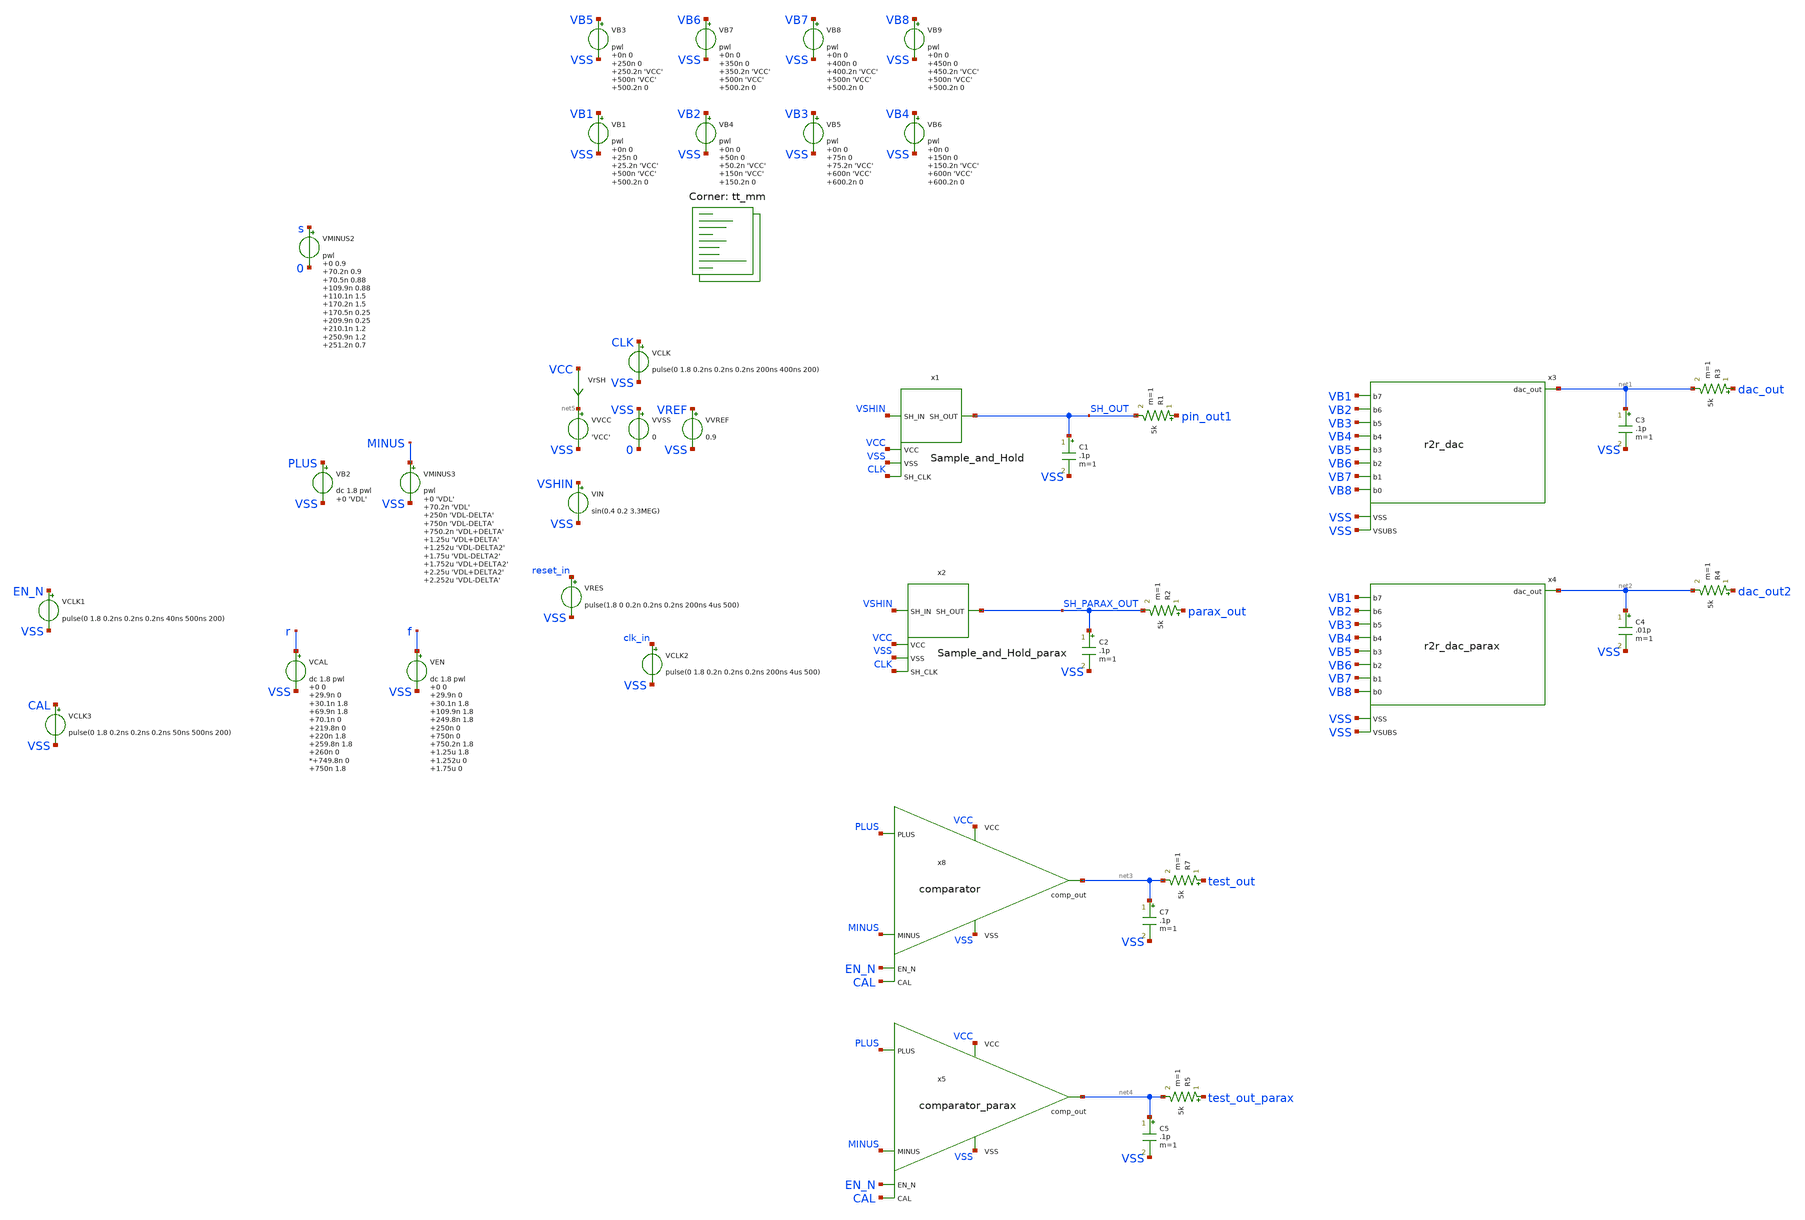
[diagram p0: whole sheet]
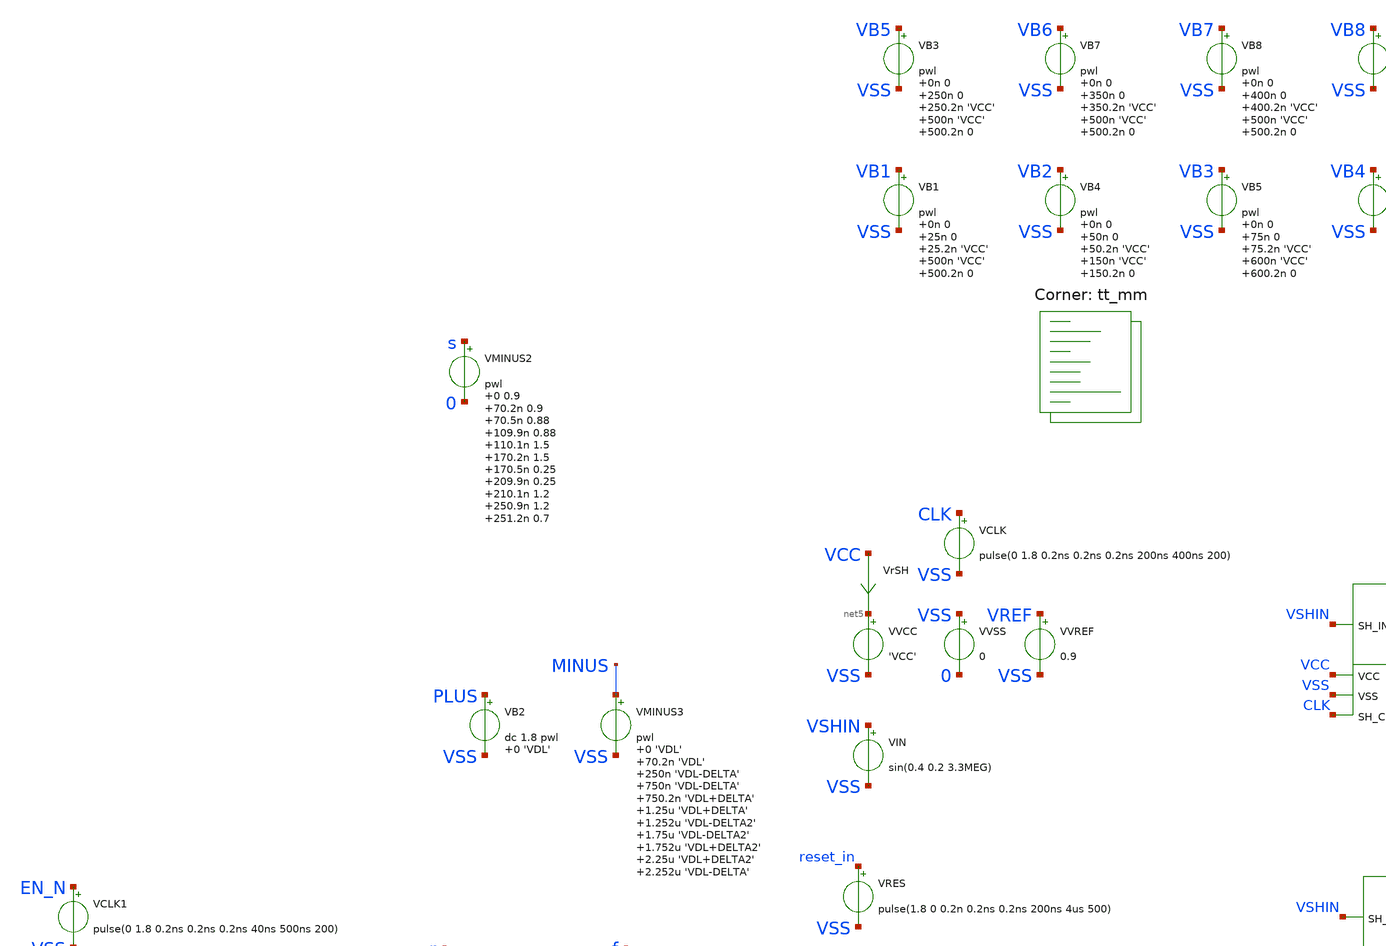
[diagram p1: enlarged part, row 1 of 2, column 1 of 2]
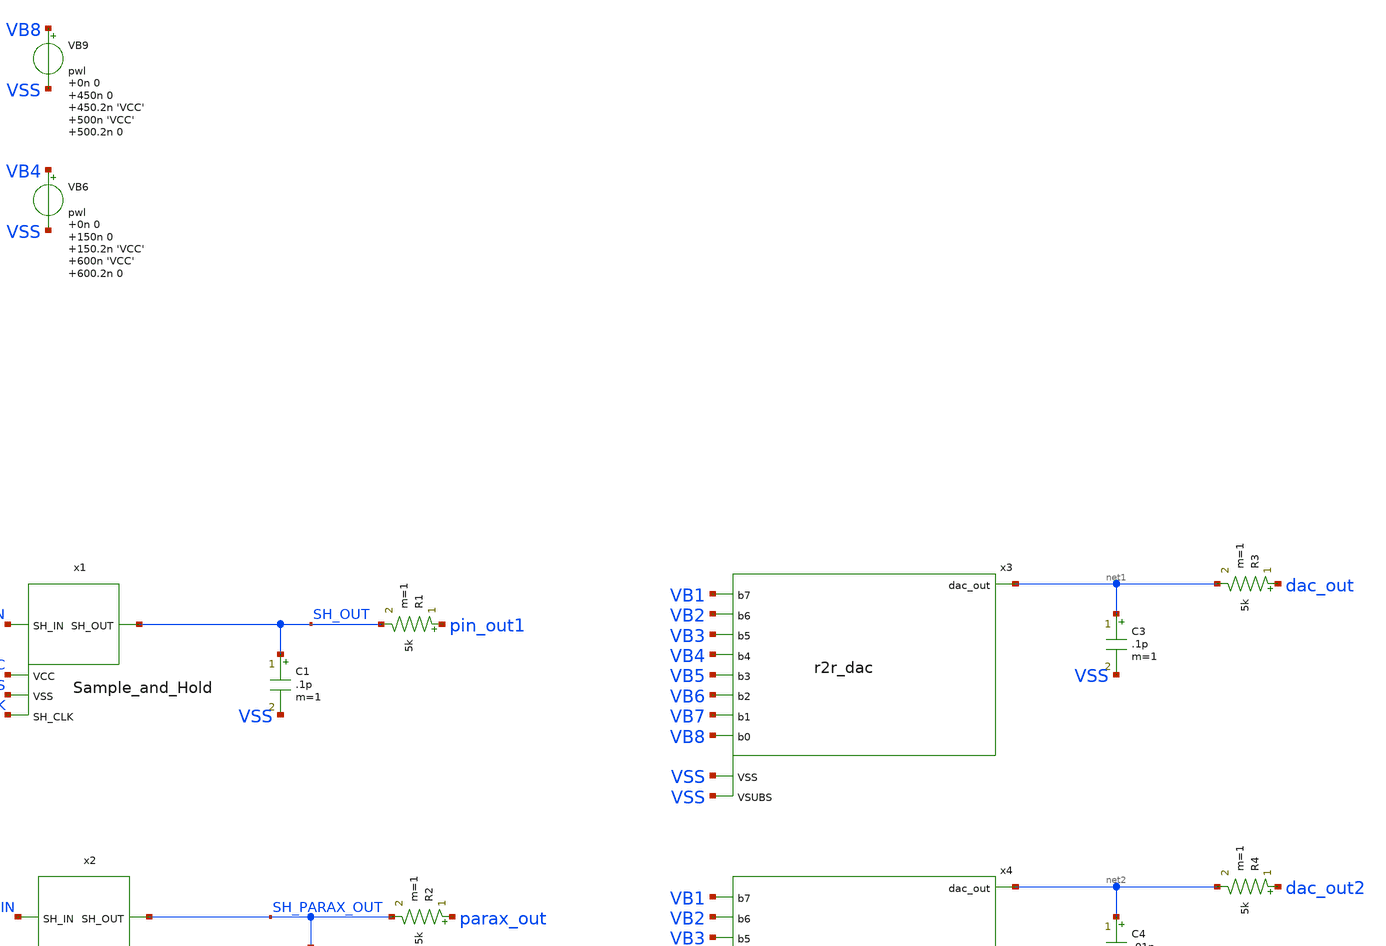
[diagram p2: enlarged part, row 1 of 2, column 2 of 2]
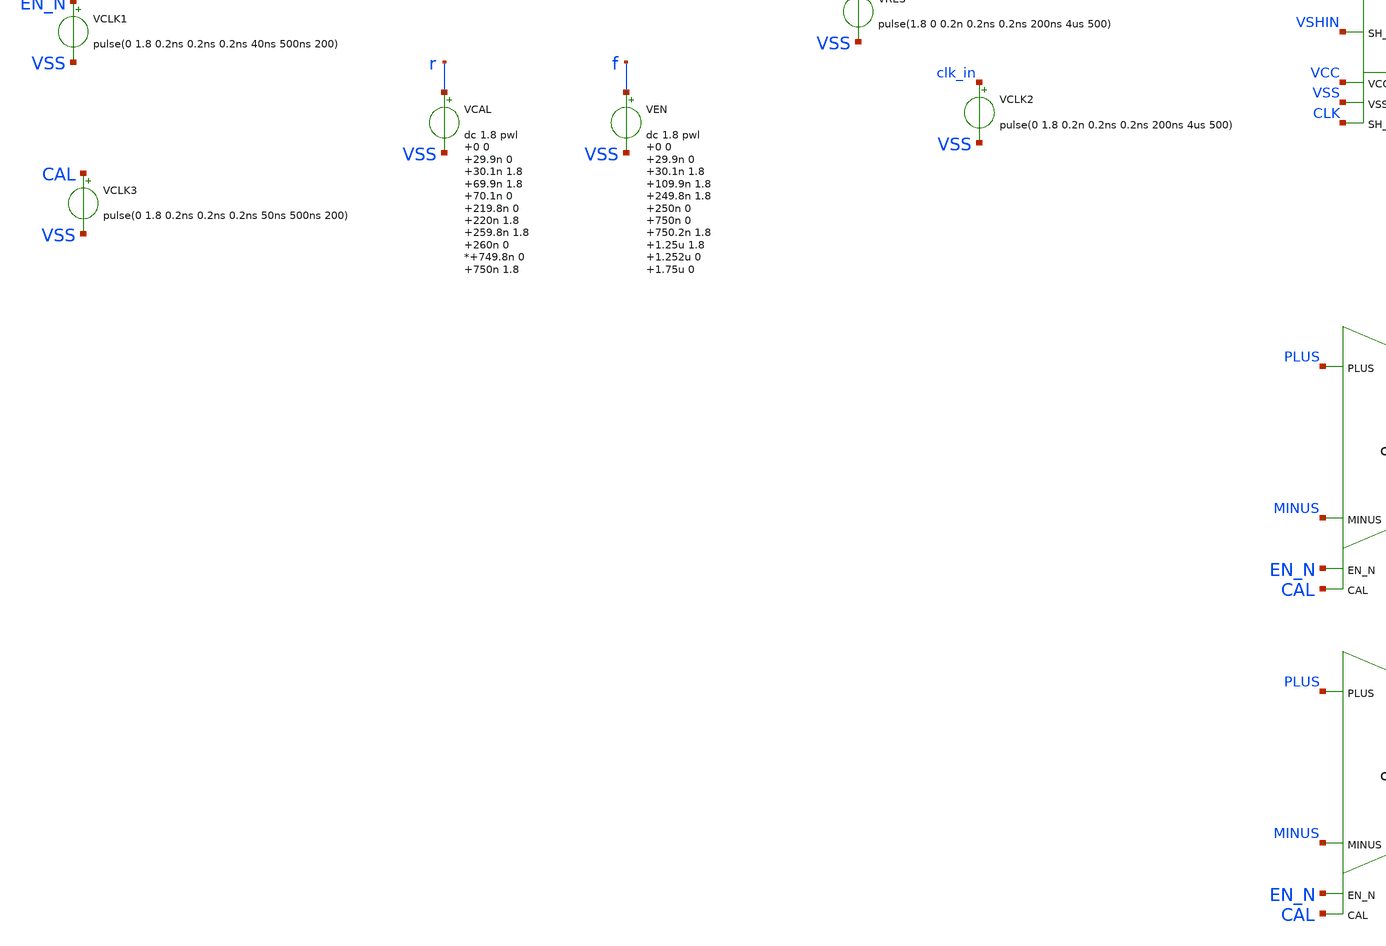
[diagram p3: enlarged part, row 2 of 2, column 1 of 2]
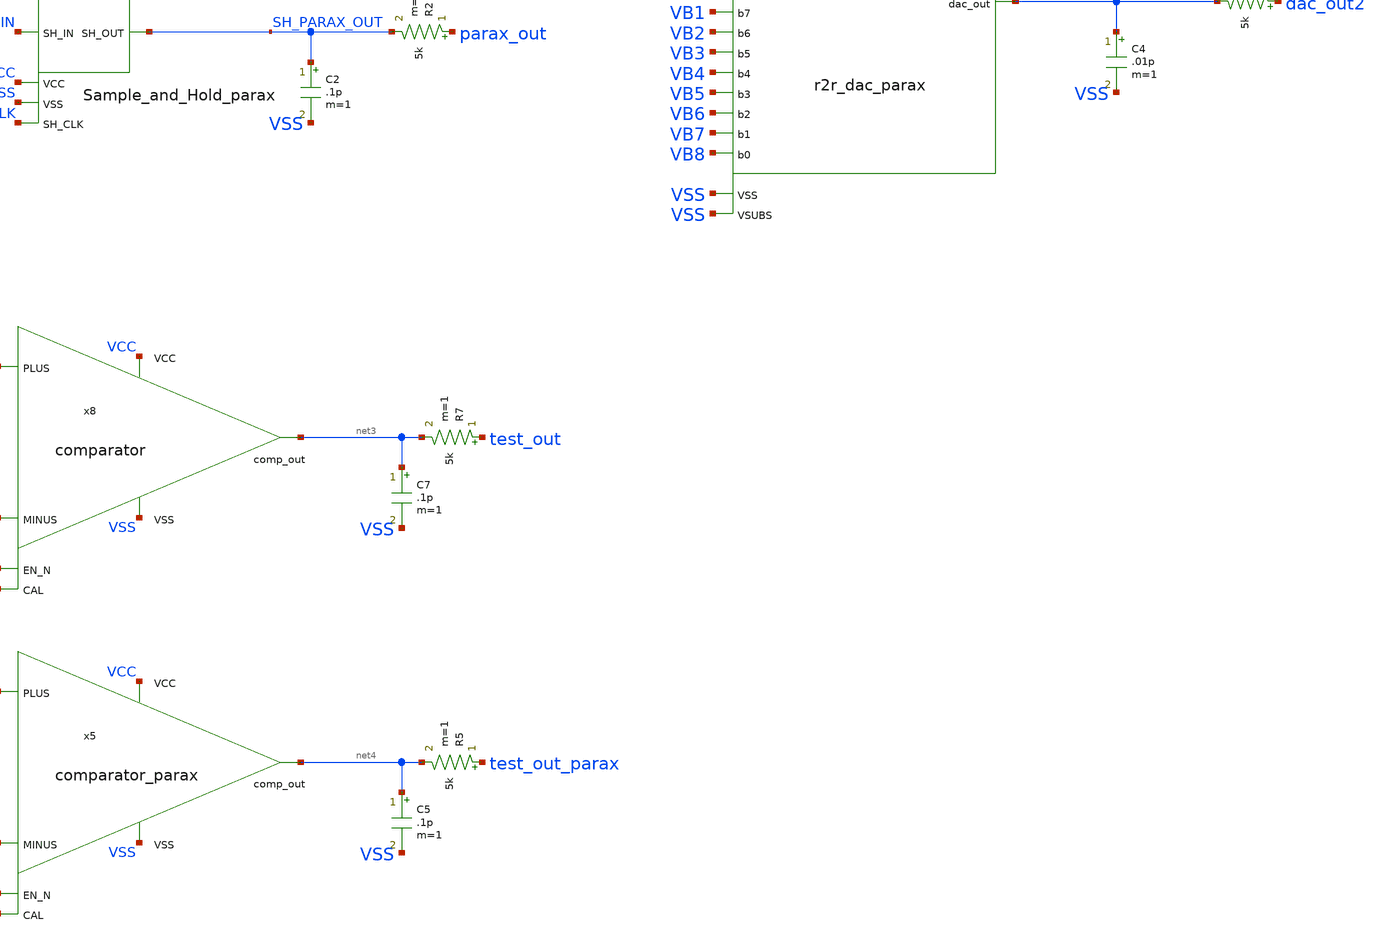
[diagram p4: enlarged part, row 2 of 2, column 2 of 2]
** sch_path: xschem/testbench.sch

.include $::SKYWATER_STDCELLS/sky130_fd_sc_hd.spice

**.subckt testbench
x1 SH_OUT VSHIN VSS VCC CLK Sample_and_Hold
VCLK CLK VSS pulse(0 1.8 0.2ns 0.2ns 0.2ns 200ns 400ns 200)
VVCC net5 VSS 'VCC'
VVSS VSS 0 0
VIN VSHIN VSS sin(0.4 0.2 3.3MEG)
VVREF VREF VSS 0.9
R1 pin_out1 SH_OUT 5k m=1
C1 SH_OUT VSS .1p m=1
VrSH VCC net5 0
.save i(vrsh)
x2 SH_PARAX_OUT VSHIN VSS VCC CLK Sample_and_Hold_parax
R2 parax_out SH_PARAX_OUT 5k m=1
C2 SH_PARAX_OUT VSS .1p m=1
x3 net1 VSS VB7 VB5 VB4 VB3 VB1 VB2 VB6 VB8 VSS r2r_dac
VB1 VB1 VSS pwl 0n 0 25n 0 25.2n 'VCC' 500n 'VCC' 500.2n 0
R3 dac_out net1 5k m=1
C3 net1 VSS .1p m=1
x4 net2 VSS VB7 VB5 VB4 VB3 VB1 VB2 VB6 VB8 VSS r2r_dac_parax
R4 dac_out2 net2 5k m=1
C4 net2 VSS .01p m=1
R7 test_out net3 5k m=1
C7 net3 VSS .1p m=1
x8 EN_N PLUS MINUS CAL net3 VCC VSS comparator
VB2 PLUS VSS dc 1.8 pwl 0 'VDL'

VCAL r VSS dc 1.8 pwl 0 0 29.9n 0 30.1n 1.8 69.9n 1.8 70.1n 0 219.8n 0 220n 1.8 259.8n 1.8 260n 0
*+749.8n 0 750n 1.8 789.8n 1.8 790n 0 2.25u 0 2.252u 1.8 2.292u 1.8 2.294u 0 3.25u 0 3.252u 1.8
*+ 3.292u 1.8 3.294u 0
VEN f VSS dc 1.8 pwl 0 0 29.9n 0 30.1n 1.8 109.9n 1.8 249.8n 1.8 250n 0 750n 0 750.2n 1.8 1.25u 1.8
+ 1.252u 0 1.75u 0 1.752u 1.8 2.25u 1.8 2.252u 0 2.75u 0 2.752u 1.8 3.25u 1.8 3.252u 0 3.75u 0 3.752u 1.8
+ 4.25u 1.8 4.252u 0 4.75u 0 4.752u 1.8
R5 test_out_parax net4 5k m=1
C5 net4 VSS .1p m=1
x5 EN_N PLUS MINUS CAL net4 VCC VSS comparator_parax
VMINUS2 s 0 pwl 0 0.9 70.2n 0.9 70.5n 0.88 109.9n 0.88 110.1n 1.5 170.2n 1.5 170.5n 0.25 209.9n 0.25
+ 210.1n 1.2 250.9n 1.2 251.2n 0.7 280.9n 0.7 281.1n 0.91 310.9n 0.91 311.1n 0.86 451.9n 0.86 452.1n 0.92
VCLK2 clk_in VSS pulse(0 1.8 0.2n 0.2ns 0.2ns 200ns 4us 500)
VRES reset_in VSS pulse(1.8 0 0.2n 0.2ns 0.2ns 200ns 4us 500)
VB4 VB2 VSS pwl 0n 0 50n 0 50.2n 'VCC' 150n 'VCC' 150.2n 0
VB5 VB3 VSS pwl 0n 0 75n 0 75.2n 'VCC' 600n 'VCC' 600.2n 0
VB6 VB4 VSS pwl 0n 0 150n 0 150.2n 'VCC' 600n 'VCC' 600.2n 0
VB3 VB5 VSS pwl 0n 0 250n 0 250.2n 'VCC' 500n 'VCC' 500.2n 0
VB7 VB6 VSS pwl 0n 0 350n 0 350.2n 'VCC' 500n 'VCC' 500.2n 0
VB8 VB7 VSS pwl 0n 0 400n 0 400.2n 'VCC' 500n 'VCC' 500.2n 0
VB9 VB8 VSS pwl 0n 0 450n 0 450.2n 'VCC' 500n 'VCC' 500.2n 0
VMINUS3 MINUS VSS pwl 0 'VDL' 70.2n 'VDL' 250n 'VDL-DELTA' 750n 'VDL-DELTA' 750.2n 'VDL+DELTA' 1.25u
+ 'VDL+DELTA' 1.252u 'VDL-DELTA2' 1.75u 'VDL-DELTA2' 1.752u 'VDL+DELTA2' 2.25u 'VDL+DELTA2' 2.252u 'VDL-DELTA'
+ 2.75u 'VDL-DELTA' 2.752u 'VDL+DELTA' 3.25u 'VDL+DELTA' 3.252u 'VDL-DELTA2' 3.75u 'VDL-DELTA2' 3.752u
+ 'VDL+DELTA2' 4.25u 'VDL+DELTA2' 4.252u 'VDL-DELTA' 4.75u 'VDL-DELTA' 4.752u 'VDL+DELTA2' 5.25u 'VDL+DELTA2'
VCLK1 EN_N VSS pulse(0 1.8 0.2ns 0.2ns 0.2ns 40ns 500ns 200)
VCLK3 CAL VSS pulse(0 1.8 0.2ns 0.2ns 0.2ns 50ns 500ns 200)
**** begin user architecture code
.lib $::SKYWATER_MODELS/sky130.lib.spice tt_mm


.option chgtol=4e-16 method=gear
.options acct list
.param VCCGAUSS = agauss(1.8, 0.05, 1)
.param VDLGAUSS = agauss(0.9, 0.23, 1)
.param TEMPGAUSS = agauss(40, 30, 1)
.param 'VCC' = 'VCCGAUSS'
.param 'VDL' = 0.1
.param 'DELTA' = 0.002
.param 'DELTA2' = 0.001
.param 'VREF' = 0.9
.option temp = 'TEMPGAUSS'
.option temp = 27
*vvcc VCC 0 1.8
*vvss VSS 0 0
*vvref VREF 0 0.9
*vclk CLK pulse(1ns 1ns 1ns 5ns 10ns 25)
*vvshin VSHIN sin(0.9 0.9 10MEG)


.control
  setseed  8
  reset
  save all
  savecurrents
  op
  write testbench.raw
  reset
  set appendwrite
  *repeat 5
    save all
    tran 1n 5.5u uic
    write testbench.raw
    set appendwrite
    reset
  *end
  quit 0
.endc

**** end user architecture code
**.ends
.end
